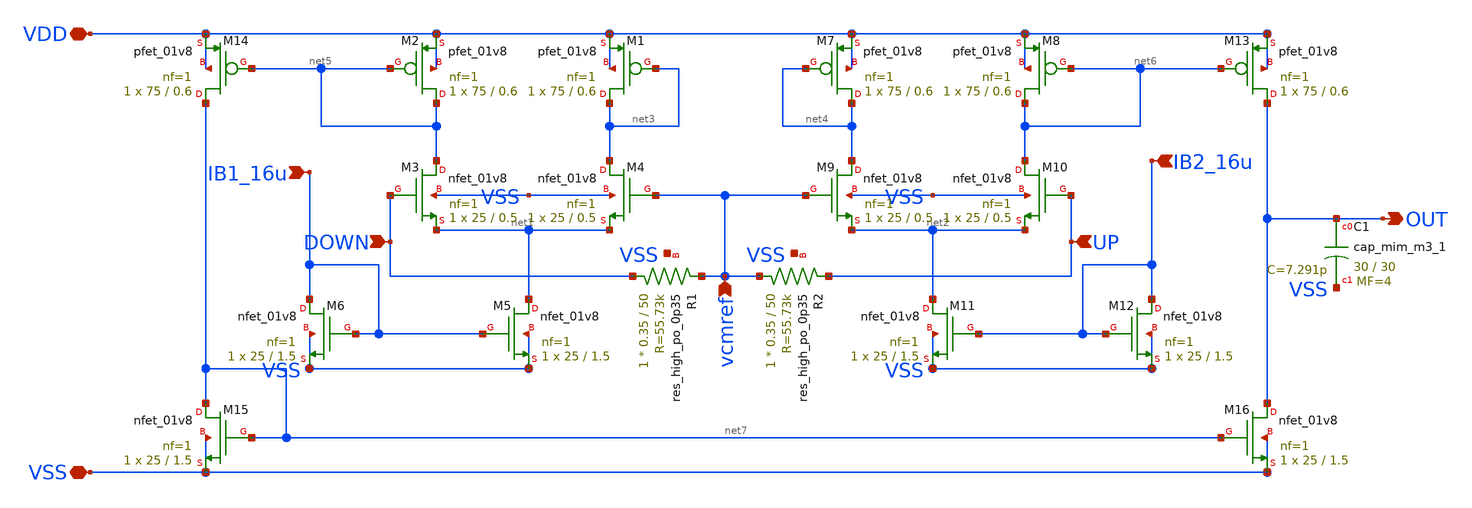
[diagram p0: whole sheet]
** sch_path: CTLE/voltage-to-i-converter.sch
**.subckt voltage-to-i-converter VDD VSS OUT IB2_16u UP DOWN IB1_16u vcmref
*.iopin VDD
*.iopin VSS
*.opin OUT
*.ipin IB2_16u
*.ipin UP
*.ipin DOWN
*.ipin IB1_16u
*.ipin vcmref
XM1 net3 net3 VDD VDD sky130_fd_pr__pfet_01v8 L=0.6 W=75 nf=1 ad='int((nf+1)/2) * W/nf * 0.29' as='int((nf+2)/2) * W/nf * 0.29'
+ pd='2*int((nf+1)/2) * (W/nf + 0.29)' ps='2*int((nf+2)/2) * (W/nf + 0.29)' nrd='0.29 / W' nrs='0.29 / W'
+ sa=0 sb=0 sd=0 mult=1 m=1
XM2 net5 net5 VDD VDD sky130_fd_pr__pfet_01v8 L=0.6 W=75 nf=1 ad='int((nf+1)/2) * W/nf * 0.29' as='int((nf+2)/2) * W/nf * 0.29'
+ pd='2*int((nf+1)/2) * (W/nf + 0.29)' ps='2*int((nf+2)/2) * (W/nf + 0.29)' nrd='0.29 / W' nrs='0.29 / W'
+ sa=0 sb=0 sd=0 mult=1 m=1
XM5 net1 IB1_16u VSS VSS sky130_fd_pr__nfet_01v8 L=1.5 W=25 nf=1 ad='int((nf+1)/2) * W/nf * 0.29' as='int((nf+2)/2) * W/nf * 0.29'
+ pd='2*int((nf+1)/2) * (W/nf + 0.29)' ps='2*int((nf+2)/2) * (W/nf + 0.29)' nrd='0.29 / W' nrs='0.29 / W'
+ sa=0 sb=0 sd=0 mult=1 m=1
XM6 IB1_16u IB1_16u VSS VSS sky130_fd_pr__nfet_01v8 L=1.5 W=25 nf=1 ad='int((nf+1)/2) * W/nf * 0.29'
+ as='int((nf+2)/2) * W/nf * 0.29' pd='2*int((nf+1)/2) * (W/nf + 0.29)' ps='2*int((nf+2)/2) * (W/nf + 0.29)'
+ nrd='0.29 / W' nrs='0.29 / W' sa=0 sb=0 sd=0 mult=1 m=1
XM7 net4 net4 VDD VDD sky130_fd_pr__pfet_01v8 L=0.6 W=75 nf=1 ad='int((nf+1)/2) * W/nf * 0.29' as='int((nf+2)/2) * W/nf * 0.29'
+ pd='2*int((nf+1)/2) * (W/nf + 0.29)' ps='2*int((nf+2)/2) * (W/nf + 0.29)' nrd='0.29 / W' nrs='0.29 / W'
+ sa=0 sb=0 sd=0 mult=1 m=1
XM8 net6 net6 VDD VDD sky130_fd_pr__pfet_01v8 L=0.6 W=75 nf=1 ad='int((nf+1)/2) * W/nf * 0.29' as='int((nf+2)/2) * W/nf * 0.29'
+ pd='2*int((nf+1)/2) * (W/nf + 0.29)' ps='2*int((nf+2)/2) * (W/nf + 0.29)' nrd='0.29 / W' nrs='0.29 / W'
+ sa=0 sb=0 sd=0 mult=1 m=1
XM11 net2 IB2_16u VSS VSS sky130_fd_pr__nfet_01v8 L=1.5 W=25 nf=1 ad='int((nf+1)/2) * W/nf * 0.29' as='int((nf+2)/2) * W/nf * 0.29'
+ pd='2*int((nf+1)/2) * (W/nf + 0.29)' ps='2*int((nf+2)/2) * (W/nf + 0.29)' nrd='0.29 / W' nrs='0.29 / W'
+ sa=0 sb=0 sd=0 mult=1 m=1
XM12 IB2_16u IB2_16u VSS VSS sky130_fd_pr__nfet_01v8 L=1.5 W=25 nf=1 ad='int((nf+1)/2) * W/nf * 0.29'
+ as='int((nf+2)/2) * W/nf * 0.29' pd='2*int((nf+1)/2) * (W/nf + 0.29)' ps='2*int((nf+2)/2) * (W/nf + 0.29)'
+ nrd='0.29 / W' nrs='0.29 / W' sa=0 sb=0 sd=0 mult=1 m=1
XM13 OUT net6 VDD VDD sky130_fd_pr__pfet_01v8 L=0.6 W=75 nf=1 ad='int((nf+1)/2) * W/nf * 0.29' as='int((nf+2)/2) * W/nf * 0.29'
+ pd='2*int((nf+1)/2) * (W/nf + 0.29)' ps='2*int((nf+2)/2) * (W/nf + 0.29)' nrd='0.29 / W' nrs='0.29 / W'
+ sa=0 sb=0 sd=0 mult=1 m=1
XM14 net7 net5 VDD VDD sky130_fd_pr__pfet_01v8 L=0.6 W=75 nf=1 ad='int((nf+1)/2) * W/nf * 0.29' as='int((nf+2)/2) * W/nf * 0.29'
+ pd='2*int((nf+1)/2) * (W/nf + 0.29)' ps='2*int((nf+2)/2) * (W/nf + 0.29)' nrd='0.29 / W' nrs='0.29 / W'
+ sa=0 sb=0 sd=0 mult=1 m=1
XM15 net7 net7 VSS VSS sky130_fd_pr__nfet_01v8 L=1.5 W=25 nf=1 ad='int((nf+1)/2) * W/nf * 0.29' as='int((nf+2)/2) * W/nf * 0.29'
+ pd='2*int((nf+1)/2) * (W/nf + 0.29)' ps='2*int((nf+2)/2) * (W/nf + 0.29)' nrd='0.29 / W' nrs='0.29 / W'
+ sa=0 sb=0 sd=0 mult=1 m=1
XM16 OUT net7 VSS VSS sky130_fd_pr__nfet_01v8 L=1.5 W=25 nf=1 ad='int((nf+1)/2) * W/nf * 0.29' as='int((nf+2)/2) * W/nf * 0.29'
+ pd='2*int((nf+1)/2) * (W/nf + 0.29)' ps='2*int((nf+2)/2) * (W/nf + 0.29)' nrd='0.29 / W' nrs='0.29 / W'
+ sa=0 sb=0 sd=0 mult=1 m=1
XR1 DOWN vcmref VSS sky130_fd_pr__res_high_po_0p35 L=50 mult=1 m=1
XR2 vcmref UP VSS sky130_fd_pr__res_high_po_0p35 L=50 mult=1 m=1
XC1 OUT VSS sky130_fd_pr__cap_mim_m3_1 W=30 L=30 MF=4 m=4
XM3 net5 DOWN net1 VSS sky130_fd_pr__nfet_01v8 L=0.5 W=25 nf=1 ad='int((nf+1)/2) * W/nf * 0.29' as='int((nf+2)/2) * W/nf * 0.29'
+ pd='2*int((nf+1)/2) * (W/nf + 0.29)' ps='2*int((nf+2)/2) * (W/nf + 0.29)' nrd='0.29 / W' nrs='0.29 / W'
+ sa=0 sb=0 sd=0 mult=1 m=1
XM4 net3 vcmref net1 VSS sky130_fd_pr__nfet_01v8 L=0.5 W=25 nf=1 ad='int((nf+1)/2) * W/nf * 0.29' as='int((nf+2)/2) * W/nf * 0.29'
+ pd='2*int((nf+1)/2) * (W/nf + 0.29)' ps='2*int((nf+2)/2) * (W/nf + 0.29)' nrd='0.29 / W' nrs='0.29 / W'
+ sa=0 sb=0 sd=0 mult=1 m=1
XM9 net4 vcmref net2 VSS sky130_fd_pr__nfet_01v8 L=0.5 W=25 nf=1 ad='int((nf+1)/2) * W/nf * 0.29' as='int((nf+2)/2) * W/nf * 0.29'
+ pd='2*int((nf+1)/2) * (W/nf + 0.29)' ps='2*int((nf+2)/2) * (W/nf + 0.29)' nrd='0.29 / W' nrs='0.29 / W'
+ sa=0 sb=0 sd=0 mult=1 m=1
XM10 net6 UP net2 VSS sky130_fd_pr__nfet_01v8 L=0.5 W=25 nf=1 ad='int((nf+1)/2) * W/nf * 0.29' as='int((nf+2)/2) * W/nf * 0.29'
+ pd='2*int((nf+1)/2) * (W/nf + 0.29)' ps='2*int((nf+2)/2) * (W/nf + 0.29)' nrd='0.29 / W' nrs='0.29 / W'
+ sa=0 sb=0 sd=0 mult=1 m=1
**.ends
.end
